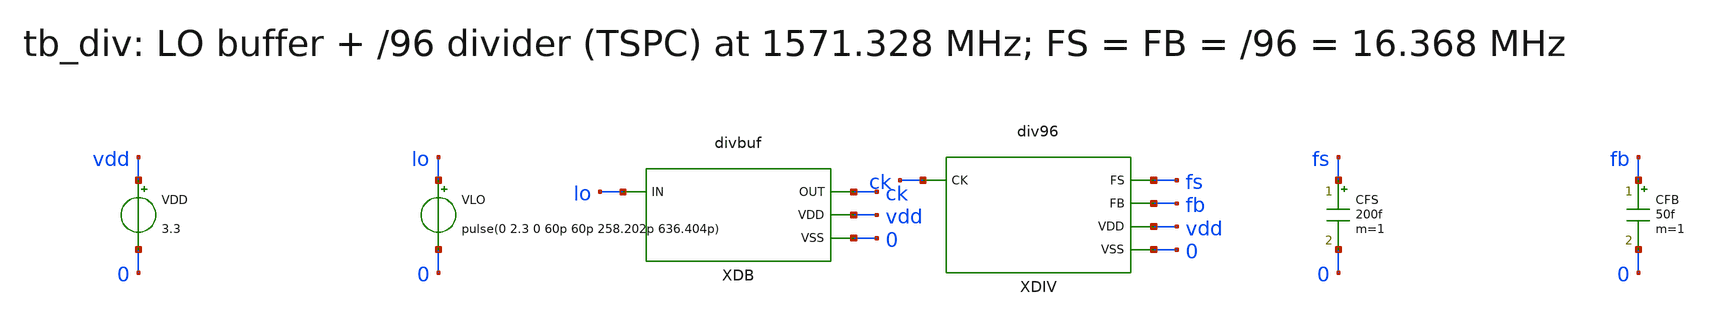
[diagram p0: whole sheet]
** sch_path: v1_claude/xschem/tb_div.sch
**.subckt tb_div
VDD vdd 0 3.3
VLO lo 0 pulse(0 2.3 0 60p 60p 258.202p 636.404p)
XDB lo ck vdd 0 divbuf
XDIV ck fs fb vdd 0 div96
CFS fs 0 200f m=1
CFB fb 0 50f m=1
**** begin user architecture code
 .include $::180MCU_MODELS/design.ngspice
.lib $::180MCU_MODELS/sm141064.ngspice typical
.lib $::180MCU_MODELS/sm141064.ngspice res_typical
.lib $::180MCU_MODELS/sm141064.ngspice mimcap_typical

.option method=gear
.control
set num_threads=1
tran 5p 400n
meas tran f1 when v(fs)=1.65 rise=2
meas tran f2 when v(fs)=1.65 rise=5
meas tran b1 when v(fb)=1.65 rise=2
meas tran b2 when v(fb)=1.65 rise=5
wrdata tb_div_wave v(fs) v(fb)
let ffs = 3/(f2-f1)
let ffb = 3/(b2-b1)
meas tran idd avg i(VDD) from=100n to=400n
echo RES ffs=$&ffs ffb=$&ffb idd=$&idd
.endc

**** end user architecture code
**.ends
.end
